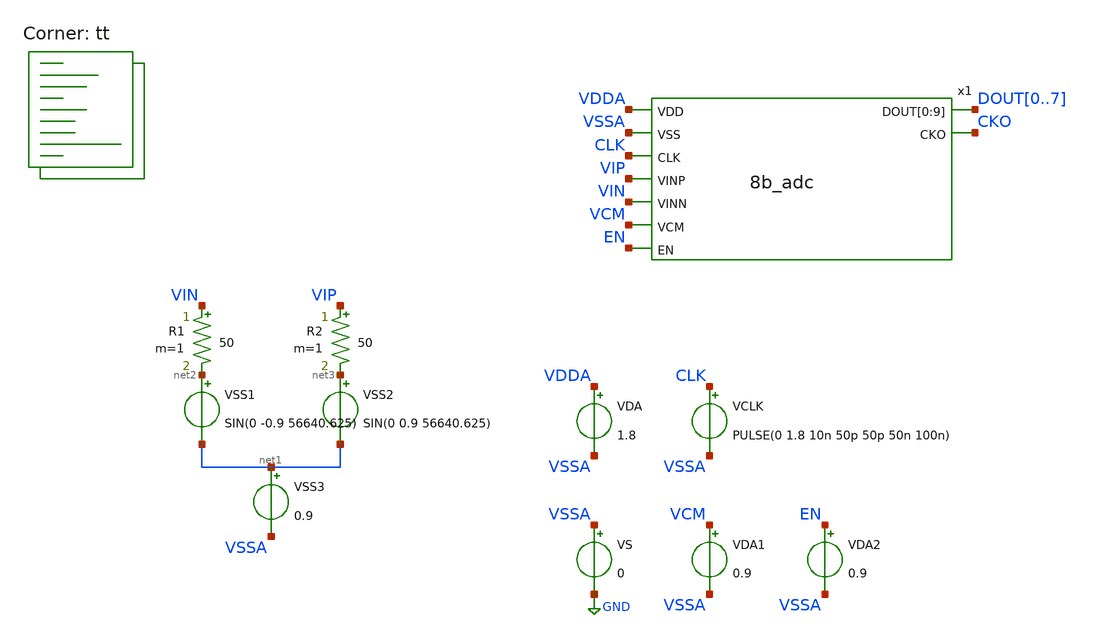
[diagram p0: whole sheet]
** sch_path: xschem/adc_tb.sch
**.subckt adc_tb
VS VSSA GND 0
VDA VDDA VSSA 1.8
VSS1 net2 net1 SIN(0 -0.9 56640.625)
VSS2 net3 net1 SIN(0 0.9 56640.625)
VSS3 net1 VSSA 0.9
VCLK CLK VSSA PULSE(0 1.8 10n 50p 50p 50n 100n)
R1 VIN net2 50 m=1
R2 VIP net3 50 m=1
x1 VDDA VSSA CLK VIP VIN VCM EN DOUT0 DOUT1 DOUT2 DOUT3 DOUT4 DOUT5 DOUT6 DOUT7 DOUT0 DOUT1 CKO
+ 8b_adc
VDA1 VCM VSSA 0.9
VDA2 EN VSSA 0.9
**** begin user architecture code

** opencircuitdesign pdks install
* .lib $::SKYWATER_MODELS/sky130.lib.spice tt
.include $PDK_ROOT/$PDK/libs.ref/sky130_fd_sc_hd/spice/sky130_fd_sc_hd.spice



.option wnflag=0
.option savecurrents
.options method=trapezoid
.options solver=iterative
.control
global netlist_dir .
set wr_singlescale
save x1.vcp x1.vcn vip vin clk vcm cko  dout0 dout1 dout2 dout3 dout4 dout5 dout6 dout7
tran 1n 20u  ; Mengubah start time menjadi 10n
remzerovec
write adc8b_tb.raw
wrdata adc8b_tb.txt cko dout0 dout1 dout2 dout3 dout4 dout5 dout6 dout7
quit 1
.endc


.lib $::SKYWATER_MODELS/sky130.lib.spice tt
**** end user architecture code
**.ends
.GLOBAL GND
.end
